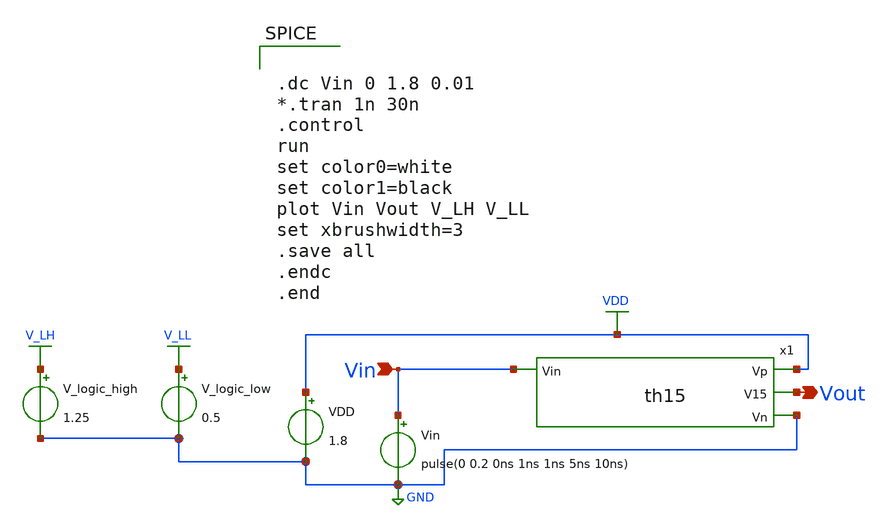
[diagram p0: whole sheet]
** sch_path: xschem/Vth_sch/Pre_layout/th15_test.sch
**.subckt th15_test Vin Vout
*.ipin Vin
*.opin Vout
VDD VDD GND 1.8
Vin Vin GND pulse(0 0.2 0ns 1ns 1ns 5ns 10ns)
V_logic_high V_LH GND 1.25
V_logic_low V_LL GND 0.5
x1 VDD Vout Vin GND th15
**** begin user architecture code


.lib /usr/local/share/pdk/sky130A/libs.tech/ngspice/sky130.lib.spice tt

.save all





.dc Vin 0 1.8 0.01
*.tran 1n 30n
.control
run
set color0=white
set color1=black
plot Vin Vout V_LH V_LL
set xbrushwidth=3
.save all
.endc
.end


**** end user architecture code
**.ends

* expanding   symbol:  /home/exotic/Desktop/ASIC_ADC/xschem/Vth_sch/Symbol/th15.sym # of pins=4
** sym_path: xschem/Vth_sch/Symbol/th15.sym
** sch_path: xschem/Vth_sch/Symbol/th15.sch
.subckt th15 Vp V15 Vin Vn
*.opin Vn
*.opin Vp
*.ipin Vin
*.opin V15
XM3 V15 net1 Vp Vp sky130_fd_pr__pfet_01v8 L=3.3 W=0.421 nf=1 ad='int((nf+1)/2) * W/nf * 0.29' as='int((nf+2)/2) * W/nf * 0.29'
+ pd='2*int((nf+1)/2) * (W/nf + 0.29)' ps='2*int((nf+2)/2) * (W/nf + 0.29)' nrd='0.29 / W' nrs='0.29 / W'
+ sa=0 sb=0 sd=0 mult=1 m=1
XM4 V15 net1 Vn Vn sky130_fd_pr__nfet_01v8 L=0.15 W=2.51 nf=1 ad='int((nf+1)/2) * W/nf * 0.29' as='int((nf+2)/2) * W/nf * 0.29'
+ pd='2*int((nf+1)/2) * (W/nf + 0.29)' ps='2*int((nf+2)/2) * (W/nf + 0.29)' nrd='0.29 / W' nrs='0.29 / W'
+ sa=0 sb=0 sd=0 mult=1 m=1
XM2 net1 Vin Vp Vp sky130_fd_pr__pfet_01v8 L=0.79 W=0.51 nf=1 ad='int((nf+1)/2) * W/nf * 0.29' as='int((nf+2)/2) * W/nf * 0.29'
+ pd='2*int((nf+1)/2) * (W/nf + 0.29)' ps='2*int((nf+2)/2) * (W/nf + 0.29)' nrd='0.29 / W' nrs='0.29 / W'
+ sa=0 sb=0 sd=0 mult=1 m=1
XM1 net1 Vin net2 Vn sky130_fd_pr__nfet_01v8 L=2.0 W=0.36 nf=1 ad='int((nf+1)/2) * W/nf * 0.29' as='int((nf+2)/2) * W/nf * 0.29'
+ pd='2*int((nf+1)/2) * (W/nf + 0.29)' ps='2*int((nf+2)/2) * (W/nf + 0.29)' nrd='0.29 / W' nrs='0.29 / W'
+ sa=0 sb=0 sd=0 mult=1 m=1
XM0 Vn Vn net2 Vp sky130_fd_pr__pfet_01v8 L=0.285 W=0.5 nf=1 ad='int((nf+1)/2) * W/nf * 0.29' as='int((nf+2)/2) * W/nf * 0.29'
+ pd='2*int((nf+1)/2) * (W/nf + 0.29)' ps='2*int((nf+2)/2) * (W/nf + 0.29)' nrd='0.29 / W' nrs='0.29 / W'
+ sa=0 sb=0 sd=0 mult=1 m=1
.ends

.GLOBAL VDD
.GLOBAL GND
.GLOBAL V_LH
.GLOBAL V_LL
.end
